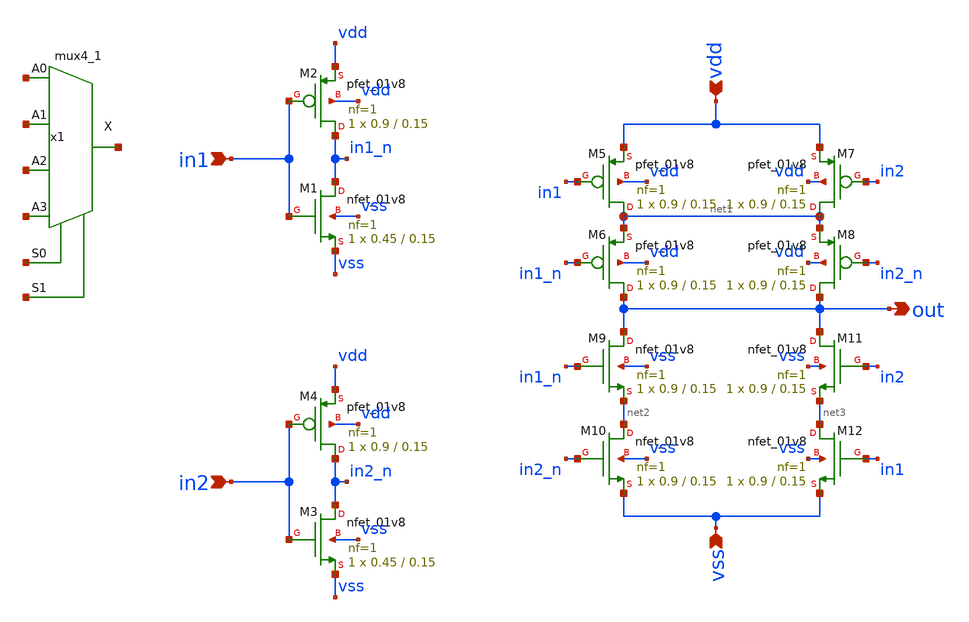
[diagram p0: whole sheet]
** sch_path: track_vlsi/celdaestandarconfig.sch
**.subckt celdaestandarconfig in1 in2 vdd vss out
*.ipin in1
*.ipin in2
*.ipin vdd
*.ipin vss
*.opin out
XM1 in1_n in1 vss vss sky130_fd_pr__nfet_01v8 L=0.15 W=0.45 nf=1 ad='int((nf+1)/2) * W/nf * 0.29' as='int((nf+2)/2) * W/nf * 0.29'
+ pd='2*int((nf+1)/2) * (W/nf + 0.29)' ps='2*int((nf+2)/2) * (W/nf + 0.29)' nrd='0.29 / W' nrs='0.29 / W'
+ sa=0 sb=0 sd=0 mult=1 m=1
XM2 in1_n in1 vdd vdd sky130_fd_pr__pfet_01v8 L=0.15 W=0.9 nf=1 ad='int((nf+1)/2) * W/nf * 0.29' as='int((nf+2)/2) * W/nf * 0.29'
+ pd='2*int((nf+1)/2) * (W/nf + 0.29)' ps='2*int((nf+2)/2) * (W/nf + 0.29)' nrd='0.29 / W' nrs='0.29 / W'
+ sa=0 sb=0 sd=0 mult=1 m=1
XM3 in2_n in2 vss vss sky130_fd_pr__nfet_01v8 L=0.15 W=0.45 nf=1 ad='int((nf+1)/2) * W/nf * 0.29' as='int((nf+2)/2) * W/nf * 0.29'
+ pd='2*int((nf+1)/2) * (W/nf + 0.29)' ps='2*int((nf+2)/2) * (W/nf + 0.29)' nrd='0.29 / W' nrs='0.29 / W'
+ sa=0 sb=0 sd=0 mult=1 m=1
XM4 in2_n in2 vdd vdd sky130_fd_pr__pfet_01v8 L=0.15 W=0.9 nf=1 ad='int((nf+1)/2) * W/nf * 0.29' as='int((nf+2)/2) * W/nf * 0.29'
+ pd='2*int((nf+1)/2) * (W/nf + 0.29)' ps='2*int((nf+2)/2) * (W/nf + 0.29)' nrd='0.29 / W' nrs='0.29 / W'
+ sa=0 sb=0 sd=0 mult=1 m=1
XM5 net1 in1 vdd vdd sky130_fd_pr__pfet_01v8 L=0.15 W=0.9 nf=1 ad='int((nf+1)/2) * W/nf * 0.29' as='int((nf+2)/2) * W/nf * 0.29'
+ pd='2*int((nf+1)/2) * (W/nf + 0.29)' ps='2*int((nf+2)/2) * (W/nf + 0.29)' nrd='0.29 / W' nrs='0.29 / W'
+ sa=0 sb=0 sd=0 mult=1 m=1
XM6 out in1_n net1 vdd sky130_fd_pr__pfet_01v8 L=0.15 W=0.9 nf=1 ad='int((nf+1)/2) * W/nf * 0.29' as='int((nf+2)/2) * W/nf * 0.29'
+ pd='2*int((nf+1)/2) * (W/nf + 0.29)' ps='2*int((nf+2)/2) * (W/nf + 0.29)' nrd='0.29 / W' nrs='0.29 / W'
+ sa=0 sb=0 sd=0 mult=1 m=1
XM7 net1 in2 vdd vdd sky130_fd_pr__pfet_01v8 L=0.15 W=0.9 nf=1 ad='int((nf+1)/2) * W/nf * 0.29' as='int((nf+2)/2) * W/nf * 0.29'
+ pd='2*int((nf+1)/2) * (W/nf + 0.29)' ps='2*int((nf+2)/2) * (W/nf + 0.29)' nrd='0.29 / W' nrs='0.29 / W'
+ sa=0 sb=0 sd=0 mult=1 m=1
XM9 out in1_n net2 vss sky130_fd_pr__nfet_01v8 L=0.15 W=0.9 nf=1 ad='int((nf+1)/2) * W/nf * 0.29' as='int((nf+2)/2) * W/nf * 0.29'
+ pd='2*int((nf+1)/2) * (W/nf + 0.29)' ps='2*int((nf+2)/2) * (W/nf + 0.29)' nrd='0.29 / W' nrs='0.29 / W'
+ sa=0 sb=0 sd=0 mult=1 m=1
XM10 net2 in2_n vss vss sky130_fd_pr__nfet_01v8 L=0.15 W=0.9 nf=1 ad='int((nf+1)/2) * W/nf * 0.29' as='int((nf+2)/2) * W/nf * 0.29'
+ pd='2*int((nf+1)/2) * (W/nf + 0.29)' ps='2*int((nf+2)/2) * (W/nf + 0.29)' nrd='0.29 / W' nrs='0.29 / W'
+ sa=0 sb=0 sd=0 mult=1 m=1
XM11 out in2 net3 vss sky130_fd_pr__nfet_01v8 L=0.15 W=0.9 nf=1 ad='int((nf+1)/2) * W/nf * 0.29' as='int((nf+2)/2) * W/nf * 0.29'
+ pd='2*int((nf+1)/2) * (W/nf + 0.29)' ps='2*int((nf+2)/2) * (W/nf + 0.29)' nrd='0.29 / W' nrs='0.29 / W'
+ sa=0 sb=0 sd=0 mult=1 m=1
XM12 net3 in1 vss vss sky130_fd_pr__nfet_01v8 L=0.15 W=0.9 nf=1 ad='int((nf+1)/2) * W/nf * 0.29' as='int((nf+2)/2) * W/nf * 0.29'
+ pd='2*int((nf+1)/2) * (W/nf + 0.29)' ps='2*int((nf+2)/2) * (W/nf + 0.29)' nrd='0.29 / W' nrs='0.29 / W'
+ sa=0 sb=0 sd=0 mult=1 m=1
XM8 out in2_n net1 vdd sky130_fd_pr__pfet_01v8 L=0.15 W=0.9 nf=1 ad='int((nf+1)/2) * W/nf * 0.29' as='int((nf+2)/2) * W/nf * 0.29'
+ pd='2*int((nf+1)/2) * (W/nf + 0.29)' ps='2*int((nf+2)/2) * (W/nf + 0.29)' nrd='0.29 / W' nrs='0.29 / W'
+ sa=0 sb=0 sd=0 mult=1 m=1
x1 net4 net5 net6 net7 net8 net9 VGND VNB VPB VPWR net10 sky130_fd_sc_hd__mux4_1
**.ends
**** begin user architecture code
[sky130_models]
**** end user architecture code
.end
